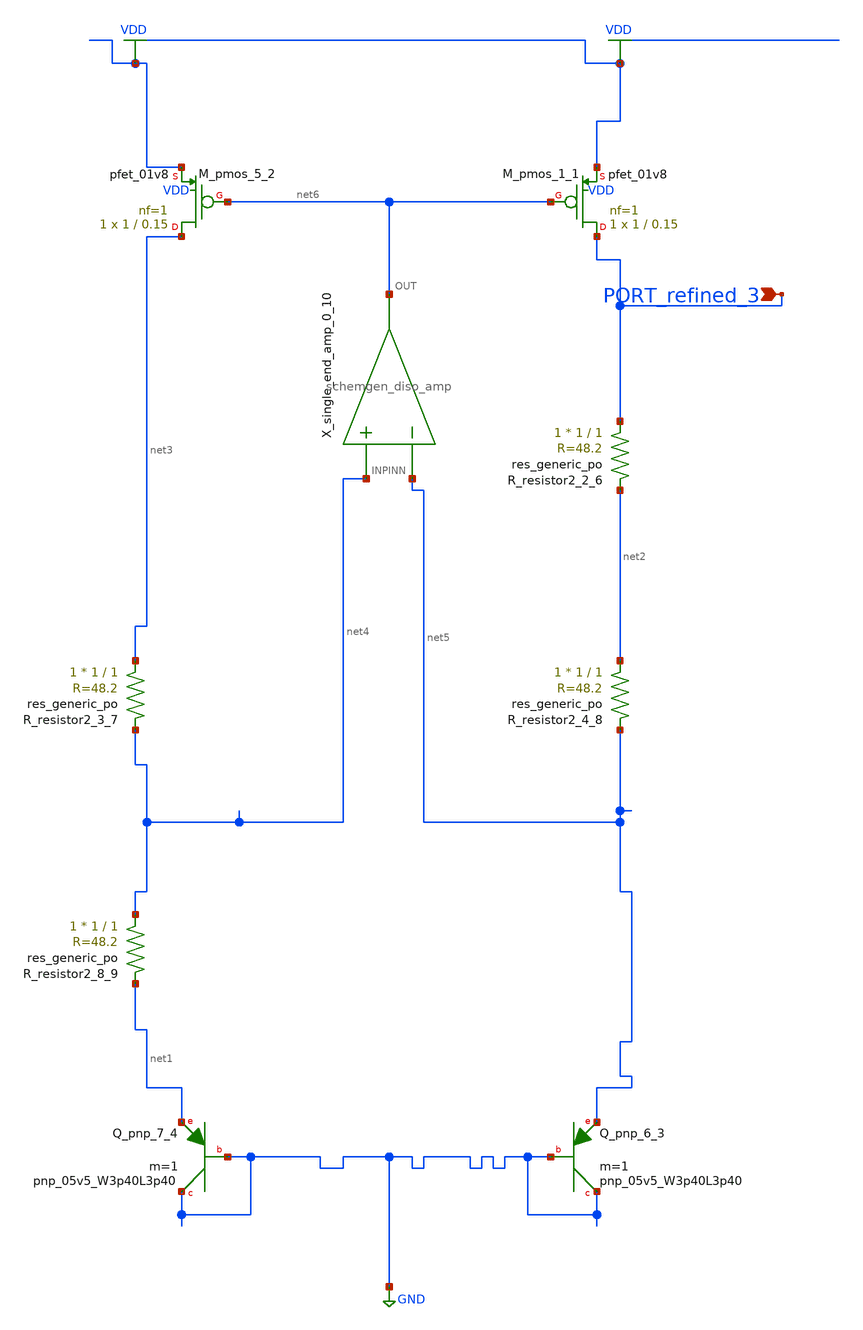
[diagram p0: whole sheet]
** sch_path: schematics/Image2Net/043.sch
**.subckt 043 PORT_refined_3
*.ipin PORT_refined_3
XM_pmos_1_1 PORT_refined_3 net6 VDD VDD sky130_fd_pr__pfet_01v8 L=0.15 W=1 nf=1 ad='int((1 + 1)/2) * 1 / 1 * 0.29'
+ as='int((1 + 2)/2) * 1 / 1 * 0.29' pd='2*int((1 + 1)/2) * (1 / 1 + 0.29)' ps='2*int((1 + 2)/2) * (1 / 1 + 0.29)'
+ nrd='0.29 / 1 ' nrs='0.29 / 1 ' sa=0 sb=0 sd=0 mult=1 m=1
XM_pmos_5_2 net3 net6 VDD VDD sky130_fd_pr__pfet_01v8 L=0.15 W=1 nf=1 ad='int((1 + 1)/2) * 1 / 1 * 0.29'
+ as='int((1 + 2)/2) * 1 / 1 * 0.29' pd='2*int((1 + 1)/2) * (1 / 1 + 0.29)' ps='2*int((1 + 2)/2) * (1 / 1 + 0.29)'
+ nrd='0.29 / 1 ' nrs='0.29 / 1 ' sa=0 sb=0 sd=0 mult=1 m=1
XQ_pnp_6_3 GND GND net5 sky130_fd_pr__pnp_05v5_W3p40L3p40 m=1
XQ_pnp_7_4 GND GND net1 sky130_fd_pr__pnp_05v5_W3p40L3p40 m=1
XR_resistor2_2_6 PORT_refined_3 net2 sky130_fd_pr__res_generic_po W=1 L=1 m=1
XR_resistor2_3_7 net3 net4 sky130_fd_pr__res_generic_po W=1 L=1 m=1
XR_resistor2_4_8 net2 net5 sky130_fd_pr__res_generic_po W=1 L=1 m=1
XR_resistor2_8_9 net4 net1 sky130_fd_pr__res_generic_po W=1 L=1 m=1
X_single_end_amp_0_10 net4 net5 net6 schemgen_diso_amp
**.ends

* expanding   symbol:  schemgen_diso_amp.sym # of pins=3
** sym_path: symbols/schemgen_diso_amp.sym
.subckt schemgen_diso_amp INP INN OUT
* SchemGen ideal op-amp: Vout = 1e5 * (V(INP) - V(INN))
E1 OUT 0 INP INN 1e5
.ends schemgen_diso_amp
.GLOBAL GND
.GLOBAL VDD
.end
